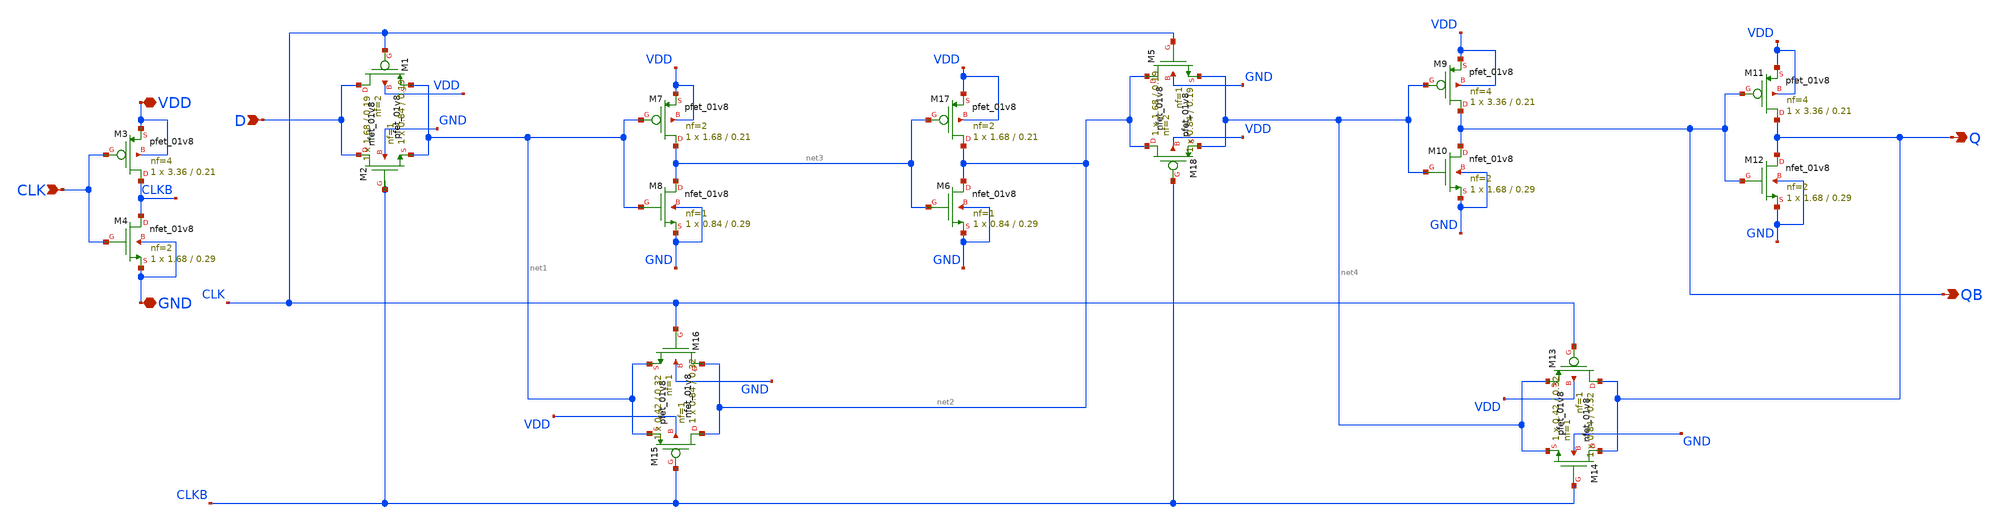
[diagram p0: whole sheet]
** sch_path: cells/DFFX4/schematic/dffx4.sch
**.subckt dffx4 VDD GND CLK D Q QB
*.iopin VDD
*.iopin GND
*.ipin CLK
*.ipin D
*.opin Q
*.opin QB
XM1 D CLK net1 VDD sky130_fd_pr__pfet_01v8 L=0.19 W=1.68 nf=2 ad='int((2 + 1)/2) * 1.68 / 2 * 0.29' as='int((2 + 2)/2) * 1.68 / 2 * 0.29'
+ pd='2*int((2 + 1)/2) * (1.68 / 2 + 0.29)' ps='2*int((2 + 2)/2) * (1.68 / 2 + 0.29)' nrd='0.29 / 1.68 '
+ nrs='0.29 / 1.68 ' sa=0 sb=0 sd=0 mult=1 m=1
XM2 D CLKB net1 GND sky130_fd_pr__nfet_01v8 L=0.19 W=0.84 nf=1 ad='int((1 + 1)/2) * 0.84 / 1 * 0.29'
+ as='int((1 + 2)/2) * 0.84 / 1 * 0.29' pd='2*int((1 + 1)/2) * (0.84 / 1 + 0.29)' ps='2*int((1 + 2)/2) * (0.84 / 1 + 0.29)'
+ nrd='0.29 / 0.84 ' nrs='0.29 / 0.84 ' sa=0 sb=0 sd=0 mult=1 m=1
XM3 CLKB CLK VDD VDD sky130_fd_pr__pfet_01v8 L=0.21 W=3.36 nf=4 ad='int((4 + 1)/2) * 3.36 / 4 * 0.29'
+ as='int((4 + 2)/2) * 3.36 / 4 * 0.29' pd='2*int((4 + 1)/2) * (3.36 / 4 + 0.29)' ps='2*int((4 + 2)/2) * (3.36 / 4 + 0.29)'
+ nrd='0.29 / 3.36 ' nrs='0.29 / 3.36 ' sa=0 sb=0 sd=0 mult=1 m=1
XM4 CLKB CLK GND GND sky130_fd_pr__nfet_01v8 L=0.29 W=1.68 nf=2 ad='int((2 + 1)/2) * 1.68 / 2 * 0.29'
+ as='int((2 + 2)/2) * 1.68 / 2 * 0.29' pd='2*int((2 + 1)/2) * (1.68 / 2 + 0.29)' ps='2*int((2 + 2)/2) * (1.68 / 2 + 0.29)'
+ nrd='0.29 / 1.68 ' nrs='0.29 / 1.68 ' sa=0 sb=0 sd=0 mult=1 m=1
XM14 Q CLKB net4 GND sky130_fd_pr__nfet_01v8 L=0.32 W=0.42 nf=1 ad='int((1 + 1)/2) * 0.42 / 1 * 0.29'
+ as='int((1 + 2)/2) * 0.42 / 1 * 0.29' pd='2*int((1 + 1)/2) * (0.42 / 1 + 0.29)' ps='2*int((1 + 2)/2) * (0.42 / 1 + 0.29)'
+ nrd='0.29 / 0.42 ' nrs='0.29 / 0.42 ' sa=0 sb=0 sd=0 mult=1 m=1
XM13 Q CLK net4 VDD sky130_fd_pr__pfet_01v8 L=0.32 W=0.84 nf=1 ad='int((1 + 1)/2) * 0.84 / 1 * 0.29'
+ as='int((1 + 2)/2) * 0.84 / 1 * 0.29' pd='2*int((1 + 1)/2) * (0.84 / 1 + 0.29)' ps='2*int((1 + 2)/2) * (0.84 / 1 + 0.29)'
+ nrd='0.29 / 0.84 ' nrs='0.29 / 0.84 ' sa=0 sb=0 sd=0 mult=1 m=1
XM7 net3 net1 VDD VDD sky130_fd_pr__pfet_01v8 L=0.21 W=1.68 nf=2 ad='int((2 + 1)/2) * 1.68 / 2 * 0.29'
+ as='int((2 + 2)/2) * 1.68 / 2 * 0.29' pd='2*int((2 + 1)/2) * (1.68 / 2 + 0.29)' ps='2*int((2 + 2)/2) * (1.68 / 2 + 0.29)'
+ nrd='0.29 / 1.68 ' nrs='0.29 / 1.68 ' sa=0 sb=0 sd=0 mult=1 m=1
XM8 net3 net1 GND GND sky130_fd_pr__nfet_01v8 L=0.29 W=0.84 nf=1 ad='int((1 + 1)/2) * 0.84 / 1 * 0.29'
+ as='int((1 + 2)/2) * 0.84 / 1 * 0.29' pd='2*int((1 + 1)/2) * (0.84 / 1 + 0.29)' ps='2*int((1 + 2)/2) * (0.84 / 1 + 0.29)'
+ nrd='0.29 / 0.84 ' nrs='0.29 / 0.84 ' sa=0 sb=0 sd=0 mult=1 m=1
XM17 net2 net3 VDD VDD sky130_fd_pr__pfet_01v8 L=0.21 W=1.68 nf=2 ad='int((2 + 1)/2) * 1.68 / 2 * 0.29'
+ as='int((2 + 2)/2) * 1.68 / 2 * 0.29' pd='2*int((2 + 1)/2) * (1.68 / 2 + 0.29)' ps='2*int((2 + 2)/2) * (1.68 / 2 + 0.29)'
+ nrd='0.29 / 1.68 ' nrs='0.29 / 1.68 ' sa=0 sb=0 sd=0 mult=1 m=1
XM6 net2 net3 GND GND sky130_fd_pr__nfet_01v8 L=0.29 W=0.84 nf=1 ad='int((1 + 1)/2) * 0.84 / 1 * 0.29'
+ as='int((1 + 2)/2) * 0.84 / 1 * 0.29' pd='2*int((1 + 1)/2) * (0.84 / 1 + 0.29)' ps='2*int((1 + 2)/2) * (0.84 / 1 + 0.29)'
+ nrd='0.29 / 0.84 ' nrs='0.29 / 0.84 ' sa=0 sb=0 sd=0 mult=1 m=1
XM9 QB net4 VDD VDD sky130_fd_pr__pfet_01v8 L=0.21 W=3.36 nf=4 ad='int((4 + 1)/2) * 3.36 / 4 * 0.29'
+ as='int((4 + 2)/2) * 3.36 / 4 * 0.29' pd='2*int((4 + 1)/2) * (3.36 / 4 + 0.29)' ps='2*int((4 + 2)/2) * (3.36 / 4 + 0.29)'
+ nrd='0.29 / 3.36 ' nrs='0.29 / 3.36 ' sa=0 sb=0 sd=0 mult=1 m=1
XM10 QB net4 GND GND sky130_fd_pr__nfet_01v8 L=0.29 W=1.68 nf=2 ad='int((2 + 1)/2) * 1.68 / 2 * 0.29'
+ as='int((2 + 2)/2) * 1.68 / 2 * 0.29' pd='2*int((2 + 1)/2) * (1.68 / 2 + 0.29)' ps='2*int((2 + 2)/2) * (1.68 / 2 + 0.29)'
+ nrd='0.29 / 1.68 ' nrs='0.29 / 1.68 ' sa=0 sb=0 sd=0 mult=1 m=1
XM11 Q QB VDD VDD sky130_fd_pr__pfet_01v8 L=0.21 W=3.36 nf=4 ad='int((4 + 1)/2) * 3.36 / 4 * 0.29' as='int((4 + 2)/2) * 3.36 / 4 * 0.29'
+ pd='2*int((4 + 1)/2) * (3.36 / 4 + 0.29)' ps='2*int((4 + 2)/2) * (3.36 / 4 + 0.29)' nrd='0.29 / 3.36 '
+ nrs='0.29 / 3.36 ' sa=0 sb=0 sd=0 mult=1 m=1
XM12 Q QB GND GND sky130_fd_pr__nfet_01v8 L=0.29 W=1.68 nf=2 ad='int((2 + 1)/2) * 1.68 / 2 * 0.29' as='int((2 + 2)/2) * 1.68 / 2 * 0.29'
+ pd='2*int((2 + 1)/2) * (1.68 / 2 + 0.29)' ps='2*int((2 + 2)/2) * (1.68 / 2 + 0.29)' nrd='0.29 / 1.68 '
+ nrs='0.29 / 1.68 ' sa=0 sb=0 sd=0 mult=1 m=1
XM5 net2 CLK net4 GND sky130_fd_pr__nfet_01v8 L=0.19 W=0.84 nf=1 ad='int((1 + 1)/2) * 0.84 / 1 * 0.29'
+ as='int((1 + 2)/2) * 0.84 / 1 * 0.29' pd='2*int((1 + 1)/2) * (0.84 / 1 + 0.29)' ps='2*int((1 + 2)/2) * (0.84 / 1 + 0.29)'
+ nrd='0.29 / 0.84 ' nrs='0.29 / 0.84 ' sa=0 sb=0 sd=0 mult=1 m=1
XM18 net2 CLKB net4 VDD sky130_fd_pr__pfet_01v8 L=0.19 W=1.68 nf=2 ad='int((2 + 1)/2) * 1.68 / 2 * 0.29'
+ as='int((2 + 2)/2) * 1.68 / 2 * 0.29' pd='2*int((2 + 1)/2) * (1.68 / 2 + 0.29)' ps='2*int((2 + 2)/2) * (1.68 / 2 + 0.29)'
+ nrd='0.29 / 1.68 ' nrs='0.29 / 1.68 ' sa=0 sb=0 sd=0 mult=1 m=1
XM15 net2 CLKB net1 VDD sky130_fd_pr__pfet_01v8 L=0.32 W=0.84 nf=1 ad='int((1 + 1)/2) * 0.84 / 1 * 0.29'
+ as='int((1 + 2)/2) * 0.84 / 1 * 0.29' pd='2*int((1 + 1)/2) * (0.84 / 1 + 0.29)' ps='2*int((1 + 2)/2) * (0.84 / 1 + 0.29)'
+ nrd='0.29 / 0.84 ' nrs='0.29 / 0.84 ' sa=0 sb=0 sd=0 mult=1 m=1
XM16 net2 CLK net1 GND sky130_fd_pr__nfet_01v8 L=0.32 W=0.42 nf=1 ad='int((1 + 1)/2) * 0.42 / 1 * 0.29'
+ as='int((1 + 2)/2) * 0.42 / 1 * 0.29' pd='2*int((1 + 1)/2) * (0.42 / 1 + 0.29)' ps='2*int((1 + 2)/2) * (0.42 / 1 + 0.29)'
+ nrd='0.29 / 0.42 ' nrs='0.29 / 0.42 ' sa=0 sb=0 sd=0 mult=1 m=1
**.ends
.end
